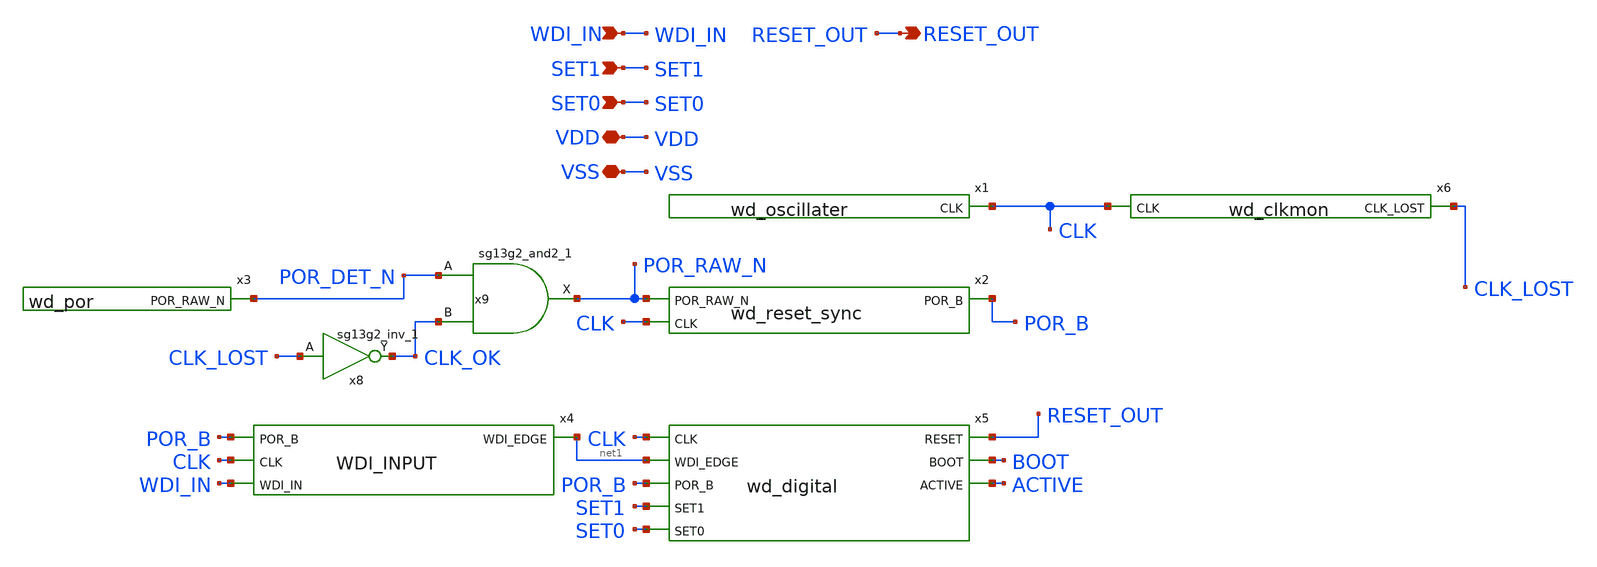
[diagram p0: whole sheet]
** sch_path: design/top/schematic/wd_watchdog.sch
**.subckt wd_watchdog SET1 SET0 WDI_IN RESET_OUT VDD VSS
*.ipin SET1
*.ipin SET0
*.ipin WDI_IN
*.opin RESET_OUT
*.iopin VDD
*.iopin VSS
x1 CLK VDD VSS wd_oscillater
x2 POR_RAW_N CLK POR_B VDD VSS wd_reset_sync
x3 POR_DET_N VDD VSS wd_por
x4 POR_B CLK WDI_IN net1 WDI_INPUT
x5 RESET_OUT BOOT CLK net1 ACTIVE POR_B SET1 SET0 VDD VSS wd_digital
x6 CLK CLK_LOST VDD VSS wd_clkmon
x8 CLK_OK CLK_LOST VDD VSS sg13g2_inv_1
x9 POR_RAW_N POR_DET_N CLK_OK VDD VSS sg13g2_and2_1
**.ends
.end
